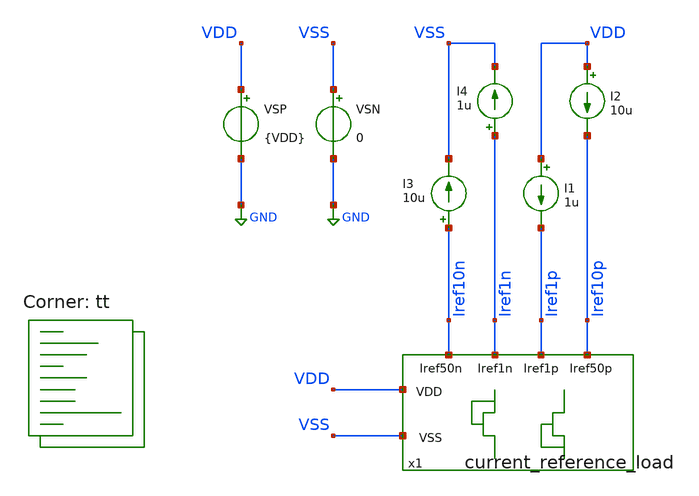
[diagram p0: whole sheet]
** sch_path: designs/current_reference_load/xschem/current_reference_load_op.sch
**.subckt current_reference_load_op
I4 Iref1n VSS 1u
VSN VSS GND 0
VSP VDD GND {VDD}
I1 VDD Iref1p 1u
I2 VDD Iref10p 10u
I3 Iref10n VSS 10u
x1 Iref1n Iref10n Iref1p Iref10p VDD VSS current_reference_load
**** begin user architecture code
.lib $::SKYWATER_MODELS/sky130.lib.spice tt



.param VDD=1.8
.save

* Operation point of the loads given ideal current outputs from the CR

*nfet
  v(@m.x1.xm3.msky130_fd_pr__nfet_01v8[vds])  v(@m.x1.xm3.msky130_fd_pr__nfet_01v8[vth])
+  @m.x1.xm3.msky130_fd_pr__nfet_01v8[id]
  v(@m.x1.xm4.msky130_fd_pr__nfet_01v8[vds])  v(@m.x1.xm4.msky130_fd_pr__nfet_01v8[vth])
+  @m.x1.xm4.msky130_fd_pr__nfet_01v8[gds]

*pfet
  v(@m.x1.xm1.msky130_fd_pr__pfet_01v8_lvt[vds])  v(@m.x1.xm1.msky130_fd_pr__pfet_01v8_lvt[vth])
+  @m.x1.xm1.msky130_fd_pr__pfet_01v8_lvt[id]
  v(@m.x1.xm2.msky130_fd_pr__pfet_01v8_lvt[vds])  v(@m.x1.xm2.msky130_fd_pr__pfet_01v8_lvt[vth])
+  @m.x1.xm2.msky130_fd_pr__pfet_01v8_lvt[gds]
  abstol=1e-14 savecurrents
.control
    save all
    op
    write CR_loads_jangarita.raw

    print v(Iref10n) v(Iref1n) v(Iref1p) v(Iref10p)
.endc



**** end user architecture code
**.ends

* expanding   symbol:
*+  /foss/designs/chipathon_2025/designs/sky130/current_reference_load/xschem/current_reference_load.sym # of pins=6
** sym_path: /foss/designs/chipathon_2025/designs/sky130/current_reference_load/xschem/current_reference_load.sym
** sch_path: /foss/designs/chipathon_2025/designs/sky130/current_reference_load/xschem/current_reference_load.sch
.subckt current_reference_load Iref1n Iref50n Iref1p Iref50p VDD VSS
*.ipin Iref1n
*.iopin VDD
*.iopin VSS
*.ipin Iref50n
*.ipin Iref1p
*.ipin Iref50p
XM1 Iref1n Iref1n VDD VDD pfet_03v3 L=2u W=5u nf=1 ad='int((nf+1)/2) * W/nf * 0.18u' as='int((nf+2)/2) * W/nf * 0.18u'
+ pd='2*int((nf+1)/2) * (W/nf + 0.18u)' ps='2*int((nf+2)/2) * (W/nf + 0.18u)' nrd='0.18u / W' nrs='0.18u / W'
+ sa=0 sb=0 sd=0 m=1
XM3 Iref1p Iref1p VSS VSS nfet_03v3 L=2u W=0.5u nf=1 ad='int((nf+1)/2) * W/nf * 0.18u' as='int((nf+2)/2) * W/nf * 0.18u'
+ pd='2*int((nf+1)/2) * (W/nf + 0.18u)' ps='2*int((nf+2)/2) * (W/nf + 0.18u)' nrd='0.18u / W' nrs='0.18u / W'
+ sa=0 sb=0 sd=0 m=1
XM2 Iref50n Iref50n VDD VDD pfet_03v3 L=2u W=5u nf=1 ad='int((nf+1)/2) * W/nf * 0.18u' as='int((nf+2)/2) * W/nf * 0.18u'
+ pd='2*int((nf+1)/2) * (W/nf + 0.18u)' ps='2*int((nf+2)/2) * (W/nf + 0.18u)' nrd='0.18u / W' nrs='0.18u / W'
+ sa=0 sb=0 sd=0 m=50
XM4 Iref50p Iref50p VSS VSS nfet_03v3 L=2u W=0.5u nf=1 ad='int((nf+1)/2) * W/nf * 0.18u' as='int((nf+2)/2) * W/nf * 0.18u'
+ pd='2*int((nf+1)/2) * (W/nf + 0.18u)' ps='2*int((nf+2)/2) * (W/nf + 0.18u)' nrd='0.18u / W' nrs='0.18u / W'
+ sa=0 sb=0 sd=0 m=50
.ends

.GLOBAL GND
.end
